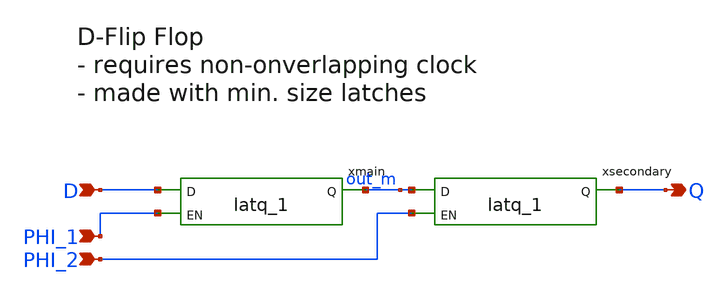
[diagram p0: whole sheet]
** sch_path: designs/switch_matrix_gf180mcu_9t5v0-main/designs/libs/core_swmatrix/DFF_2phase_1.sch
**.subckt DFF_2phase_1 D PHI_1 PHI_2 Q
*.ipin D
*.ipin PHI_1
*.ipin PHI_2
*.opin Q
xmain D PHI_1 out_m VDDd VDDd VSSd VSSd gf180mcu_fd_sc_mcu9t5v0__latq_1
xsecondary out_m PHI_2 Q VDDd VDDd VSSd VSSd gf180mcu_fd_sc_mcu9t5v0__latq_1
**.ends
.end
